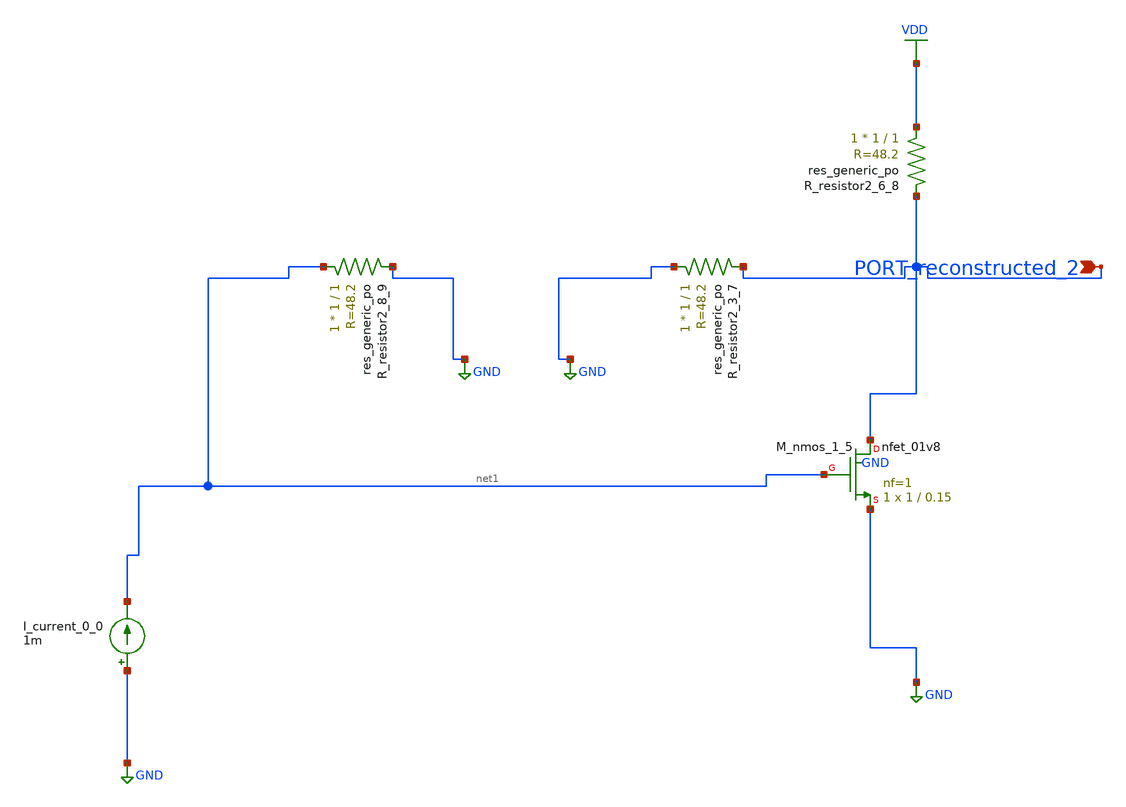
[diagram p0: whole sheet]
** sch_path: schematics/AMSNet/579.sch
**.subckt 579 PORT_reconstructed_2
*.ipin PORT_reconstructed_2
I_current_0_0 GND net1 1m
XM_nmos_1_5 PORT_reconstructed_2 net1 GND GND sky130_fd_pr__nfet_01v8 L=0.15 W=1 nf=1 ad='int((1 + 1)/2) * 1 / 1 * 0.29'
+ as='int((1 + 2)/2) * 1 / 1 * 0.29' pd='2*int((1 + 1)/2) * (1 / 1 + 0.29)' ps='2*int((1 + 2)/2) * (1 / 1 + 0.29)'
+ nrd='0.29 / 1 ' nrs='0.29 / 1 ' sa=0 sb=0 sd=0 mult=1 m=1
XR_resistor2_3_7 GND PORT_reconstructed_2 sky130_fd_pr__res_generic_po W=1 L=1 m=1
XR_resistor2_6_8 VDD PORT_reconstructed_2 sky130_fd_pr__res_generic_po W=1 L=1 m=1
XR_resistor2_8_9 net1 GND sky130_fd_pr__res_generic_po W=1 L=1 m=1
**.ends
.GLOBAL GND
.GLOBAL VDD
.end
